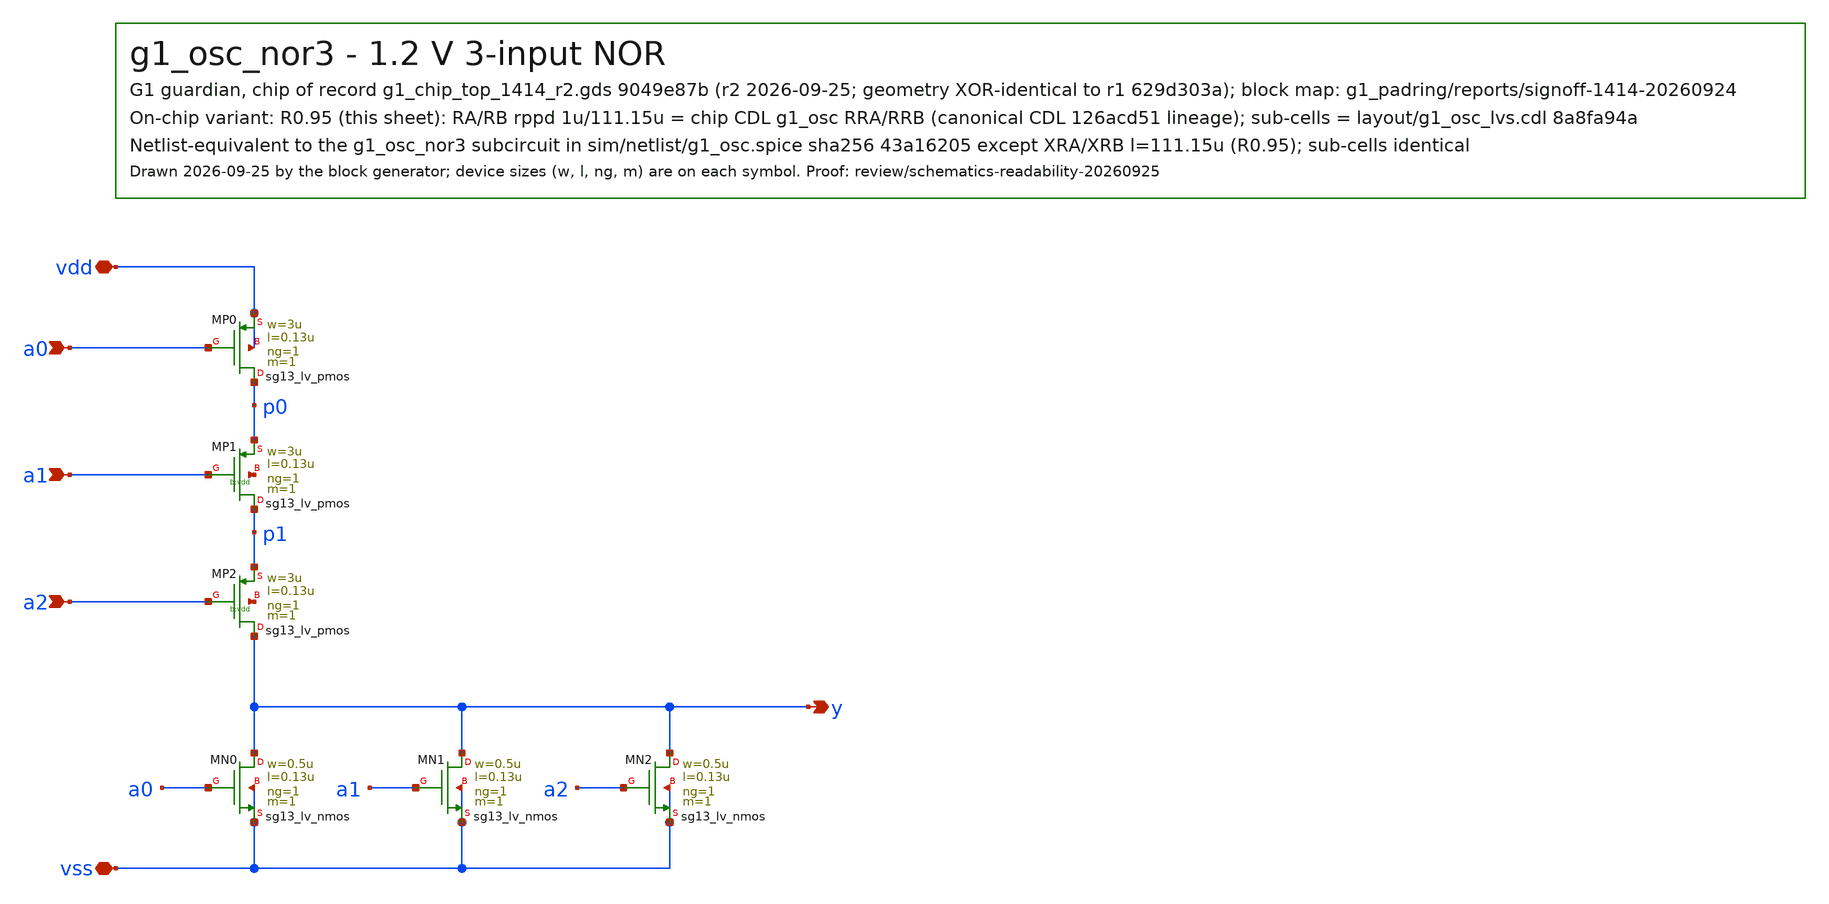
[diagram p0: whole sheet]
** sch_path: designs/g1-guardian/blocks/g1_osc/schematic/g1_osc_nor3.sch
**.subckt g1_osc_nor3 a0 a1 a2 y vdd vss
*.ipin a0
*.ipin a1
*.ipin a2
*.opin y
*.iopin vdd
*.iopin vss
XMP0 p0 a0 vdd vdd sg13_lv_pmos w=3u l=0.13u ng=1 m=1 mm_ok=1
XMP1 p1 a1 p0 vdd sg13_lv_pmos w=3u l=0.13u ng=1 m=1 mm_ok=1
XMP2 y a2 p1 vdd sg13_lv_pmos w=3u l=0.13u ng=1 m=1 mm_ok=1
XMN0 y a0 vss vss sg13_lv_nmos w=0.5u l=0.13u ng=1 m=1 mm_ok=1
XMN1 y a1 vss vss sg13_lv_nmos w=0.5u l=0.13u ng=1 m=1 mm_ok=1
XMN2 y a2 vss vss sg13_lv_nmos w=0.5u l=0.13u ng=1 m=1 mm_ok=1
**.ends
.end
